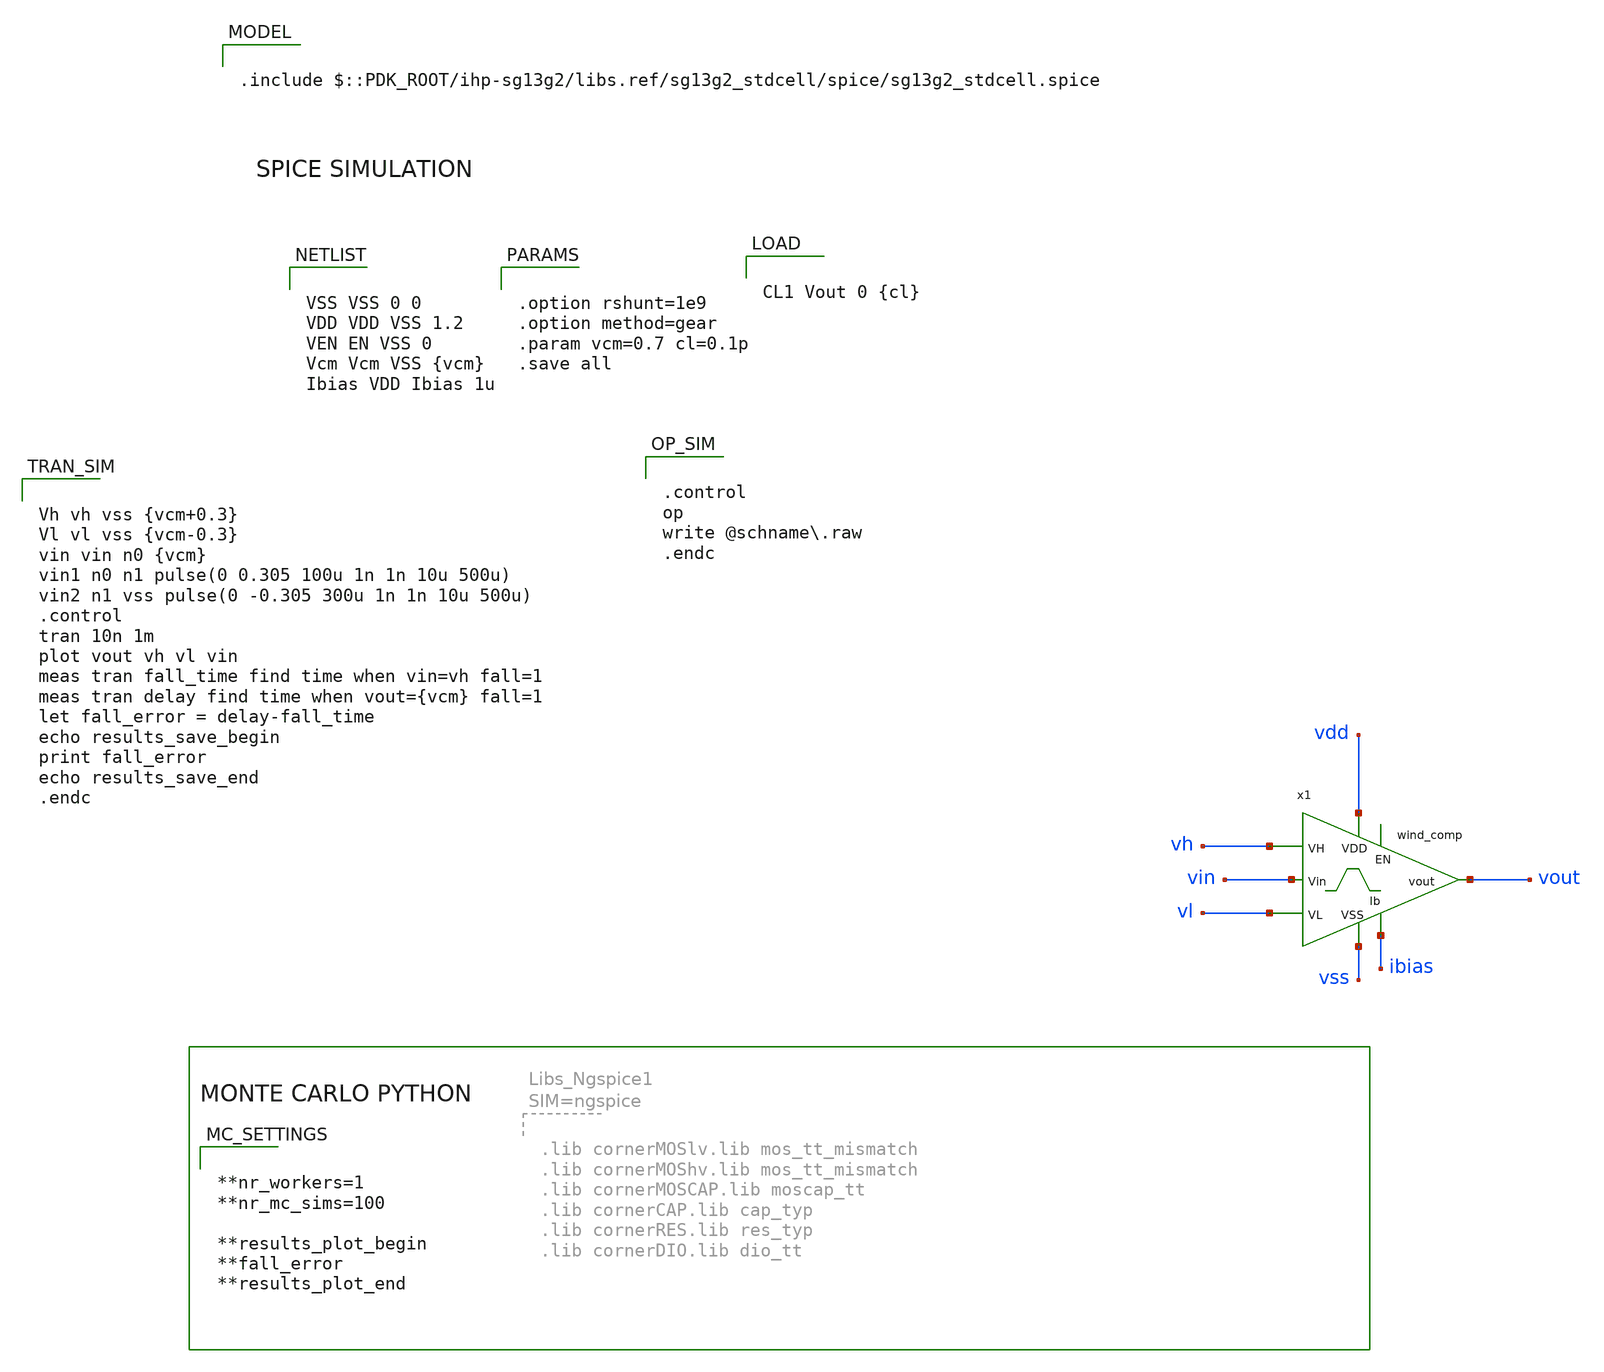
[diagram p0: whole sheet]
** sch_path: schematic/xschem/wind_comp/wind_comp_tb.sch

.include $::PDK_ROOT/ihp-sg13g2/libs.ref/sg13g2_stdcell/spice/sg13g2_stdcell.spice


**.subckt wind_comp_tb
x1 vdd vh vout vin vl ibias vss wind_comp
**** begin user architecture code


VSS VSS 0 0
VDD VDD VSS 1.2
VEN EN VSS 0
Vcm Vcm VSS {vcm}
Ibias VDD Ibias 1u



.control
op
write @schname.raw
.endc




.lib cornerMOSlv.lib mos_tt
.lib cornerMOShv.lib mos_tt
.lib cornerMOSCAP.lib moscap_tt
.lib cornerCAP.lib cap_typ
.lib cornerRES.lib res_typ
.lib cornerDIO.lib dio_tt





.option rshunt=1e9
.option method=gear
.param vcm=0.7 cl=0.1p
.save all




CL1 Vout 0 {cl}



.include @schname.save



Vh vh vss {vcm+0.3}
Vl vl vss {vcm-0.3}
vin vin n0 {vcm}
vin1 n0 n1 pulse(0 0.305 100u 1n 1n 10u 500u)
vin2 n1 vss pulse(0 -0.305 300u 1n 1n 10u 500u)
.control
tran 10n 1m
plot vout vh vl vin
meas tran fall_time find time when vin=vh fall=1
meas tran delay find time when vout={vcm} fall=1
let fall_error = delay-fall_time
echo results_save_begin
print fall_error
echo results_save_end
.endc




**nr_workers=1
**nr_mc_sims=100

**results_plot_begin
**fall_error
**results_plot_end


**** end user architecture code
**.ends

* expanding   symbol:  /foss/designs/ic_design/chipaloza/schema/wind_comp/wind_comp.sym # of pins=7
** sym_path: schematic/xschem/wind_comp/wind_comp.sym
** sch_path: schematic/xschem/wind_comp/wind_comp.sch
.subckt wind_comp vdd vh vout vin vl ibias vss
*.iopin vdd
*.iopin vout
*.iopin vl
*.iopin vh
*.iopin ibias
*.iopin vss
*.iopin vin
x1 vdd net1 vh vin ibias vss comparator
x2 vdd net2 vin vl ibias vss comparator
x3 vout net1 net2 VDD VSS sg13g2_nand2_1
XM12 ibias ibias vss vss sg13_lv_nmos w=2u l=5u ng=1 m=1 mm_ok=1
.ends


* expanding   symbol:  /foss/designs/ic_design/chipaloza/schema/comparator/comparator.sym # of
*+ pins=6
** sym_path: schematic/xschem/comparator/comparator.sym
** sch_path: schematic/xschem/comparator/comparator.sch
.subckt comparator vdd vout v- v+ iout vss
*.iopin vdd
*.iopin vss
*.iopin v-
*.iopin v+
*.iopin iout
*.iopin vout
XM6 votap v+ net1 vss sg13_lv_nmos w=0.26u l=3u ng=1 m=2 mm_ok=1
XM8 vdd votap votap vdd sg13_lv_pmos w=0.35u l=1u ng=1 m=2 mm_ok=1
XM9 votan v- net1 vss sg13_lv_nmos w=0.26u l=3u ng=1 m=2 mm_ok=1
XM10 vdd votan votan vdd sg13_lv_pmos w=0.35u l=1u ng=1 m=2 mm_ok=1
XM11 net1 iout vss vss sg13_lv_nmos w=2u l=5u ng=1 m=2 mm_ok=1
x1 vdd votan vom vop vss vss decision_circuit
x2 vdd votap vop vom vss vss decision_circuit
x3 net3 net2 VDD VSS sg13g2_inv_16
x4 vdd iout vop vom net2 vss final_stage_ota
x5 vout net3 VDD VSS sg13g2_inv_16
.ends


* expanding   symbol:
*+  /foss/designs/ic_design/chipaloza/schema/decision_circuit/decision_circuit.sym # of pins=6
** sym_path: schematic/xschem/decision_circuit/decision_circuit.sym
** sch_path: schematic/xschem/decision_circuit/decision_circuit.sch
.subckt decision_circuit vdd vota vout vota_n vss shift
*.iopin vota
*.iopin shift
*.iopin vota_n
*.iopin vdd
*.iopin vss
*.iopin vout
XM1 vout vota vdd vdd sg13_lv_pmos w=0.7u l=1u ng=1 m=1 mm_ok=1
XM2 vout vout shift vss sg13_lv_nmos w=0.26u l=10u ng=1 m=2 mm_ok=1
XM3 vout vota_n shift vss sg13_lv_nmos w=0.26u l=10u ng=1 m=2 mm_ok=1
.ends


* expanding   symbol:  /foss/designs/ic_design/chipaloza/schema/final_stage_ota/final_stage_ota.sym
*+ # of pins=6
** sym_path: schematic/xschem/final_stage_ota/final_stage_ota.sym
** sch_path: schematic/xschem/final_stage_ota/final_stage_ota.sch
.subckt final_stage_ota vdd iout vop vom vout vss
*.iopin vdd
*.iopin vom
*.iopin vop
*.iopin vss
*.iopin vout
*.iopin iout
XM1 vdd ibp vt vdd sg13_lv_pmos w=1u l=3u ng=1 m=2 mm_ok=1
XM2 net1 net1 vss vss sg13_lv_nmos w=0.15u l=3u ng=1 m=2 mm_ok=1
XM3 vt vom net1 vdd sg13_lv_pmos w=3.12u l=1u ng=1 m=2 mm_ok=1
XM4 vout net1 vss vss sg13_lv_nmos w=0.15u l=3u ng=1 m=2 mm_ok=1
XM5 vt vop vout vdd sg13_lv_pmos w=3.12u l=1u ng=1 m=2 mm_ok=1
XM6 ibp iout vss vss sg13_lv_nmos w=2u l=5u ng=1 m=1 mm_ok=1
XM7 vdd ibp ibp vdd sg13_lv_pmos w=1u l=3u ng=1 m=1 mm_ok=1
.ends

.end
